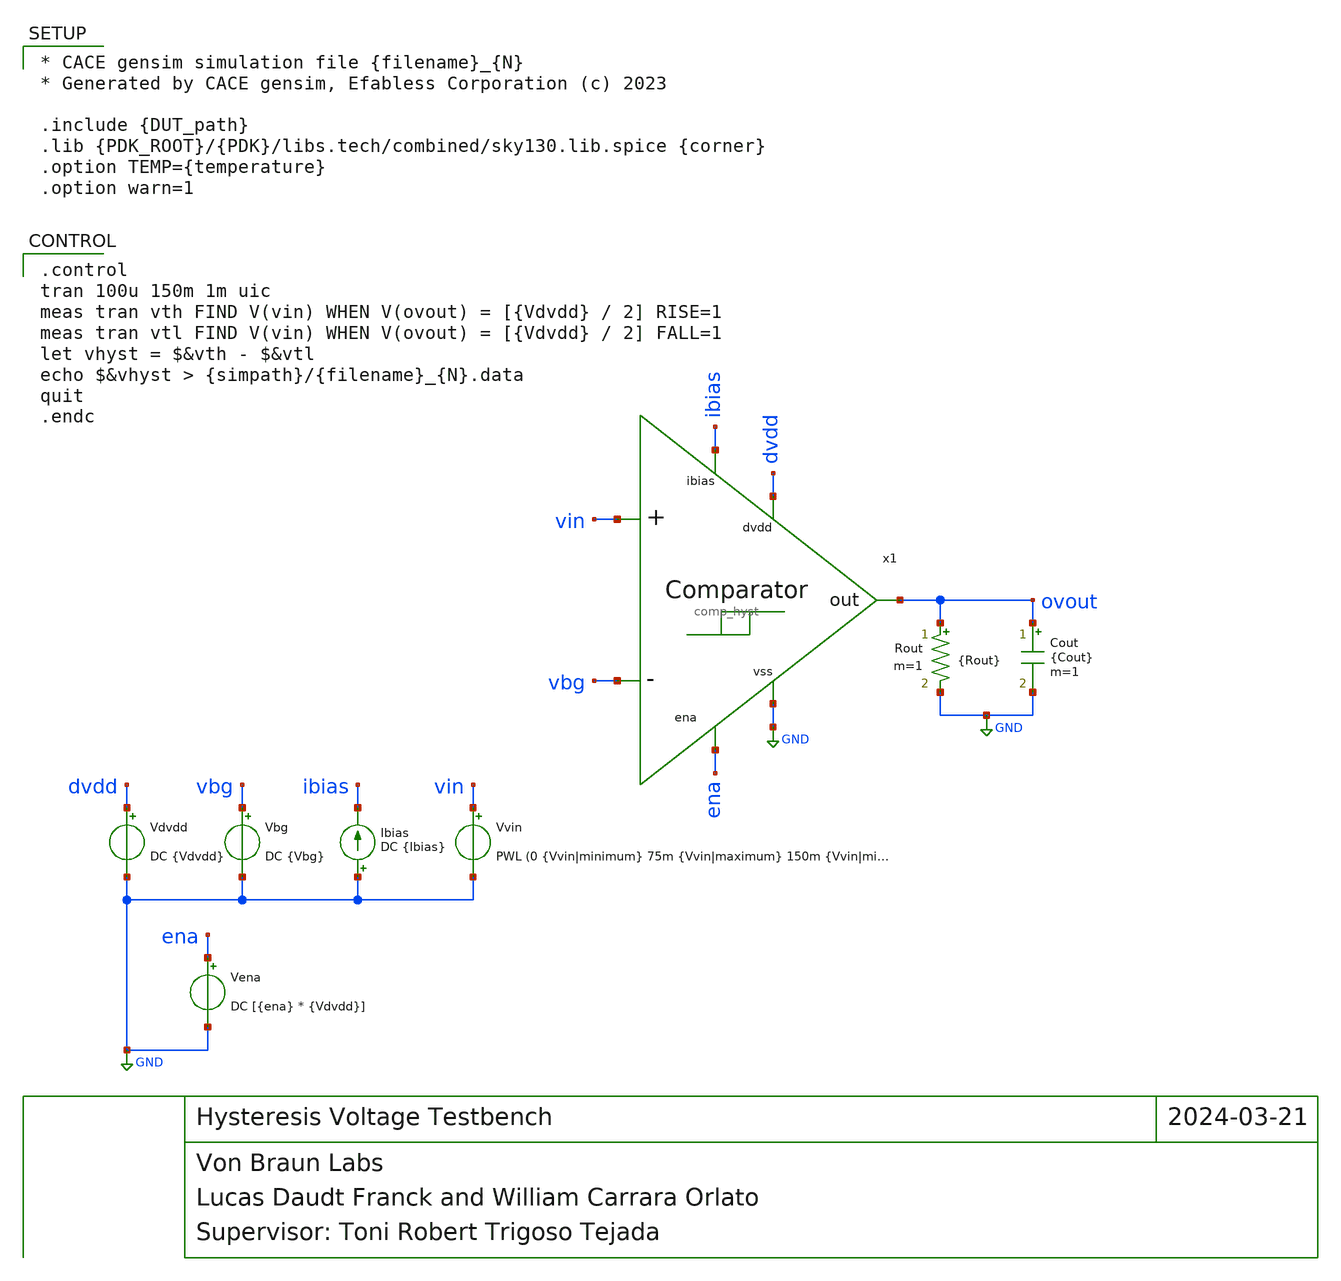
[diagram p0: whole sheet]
** sch_path: blocks/comp_hyst/cace/tb_vhyst.sch
* blocks/comp_hyst/xschem/comp_hyst.sch:
* Design under the Apache License Version 2.0 (Jan. 2004)
**.subckt tb_vhyst
Vvin vin GND PWL (0 {Vvin|minimum} 75m {Vvin|maximum} 150m {Vvin|minimum})
Vdvdd dvdd GND DC {Vdvdd}
Vbg vbg GND DC {Vbg}
Ibias GND ibias DC {Ibias}
Vena ena GND DC [{ena} * {Vdvdd}]
Cout ovout GND {Cout} m=1
Rout ovout GND {Rout} m=1
x1 dvdd ovout vbg vin ena ibias GND comp_hyst
**** begin user architecture code

* CACE gensim simulation file {filename}_{N}
* Generated by CACE gensim, Efabless Corporation (c) 2023

.include {DUT_path}
.lib {PDK_ROOT}/{PDK}/libs.tech/combined/sky130.lib.spice {corner}
.option TEMP={temperature}
.option warn=1



.control
tran 100u 150m 1m uic
meas tran vth FIND V(vin) WHEN V(ovout) = [{Vdvdd} / 2] RISE=1
meas tran vtl FIND V(vin) WHEN V(ovout) = [{Vdvdd} / 2] FALL=1
let vhyst = $&vth - $&vtl
echo $&vhyst > {simpath}/{filename}_{N}.data
quit
.endc


**** end user architecture code
**.ends

* expanding   symbol:  /home/vblabs/Music/blocks/comp_hyst/xschem/comp_hyst.sym # of pins=7
** sym_path: blocks/comp_hyst/xschem/comp_hyst.sym
** sch_path: blocks/comp_hyst/xschem/comp_hyst.sch
.subckt comp_hyst dvdd out vref vin ena ibias vss
*.iopin dvdd
*.ipin vref
*.ipin vin
*.opin out
*.ipin ibias
*.ipin ena
*.iopin vss
XM5[0] net3 net4 dvdd dvdd sky130_fd_pr__pfet_01v8 L=8 W=1 nf=1 ad='int((nf+1)/2) * W/nf * 0.29' as='int((nf+2)/2) * W/nf * 0.29'
+ pd='2*int((nf+1)/2) * (W/nf + 0.29)' ps='2*int((nf+2)/2) * (W/nf + 0.29)' nrd='0.29 / W' nrs='0.29 / W'
+ sa=0 sb=0 sd=0 mult=1 m=1
XM5[1] net3 net4 dvdd dvdd sky130_fd_pr__pfet_01v8 L=8 W=1 nf=1 ad='int((nf+1)/2) * W/nf * 0.29' as='int((nf+2)/2) * W/nf * 0.29'
+ pd='2*int((nf+1)/2) * (W/nf + 0.29)' ps='2*int((nf+2)/2) * (W/nf + 0.29)' nrd='0.29 / W' nrs='0.29 / W'
+ sa=0 sb=0 sd=0 mult=1 m=1
XM2[0] net4 net4 dvdd dvdd sky130_fd_pr__pfet_01v8 L=8 W=1 nf=1 ad='int((nf+1)/2) * W/nf * 0.29' as='int((nf+2)/2) * W/nf * 0.29'
+ pd='2*int((nf+1)/2) * (W/nf + 0.29)' ps='2*int((nf+2)/2) * (W/nf + 0.29)' nrd='0.29 / W' nrs='0.29 / W'
+ sa=0 sb=0 sd=0 mult=1 m=1
XM2[1] net4 net4 dvdd dvdd sky130_fd_pr__pfet_01v8 L=8 W=1 nf=1 ad='int((nf+1)/2) * W/nf * 0.29' as='int((nf+2)/2) * W/nf * 0.29'
+ pd='2*int((nf+1)/2) * (W/nf + 0.29)' ps='2*int((nf+2)/2) * (W/nf + 0.29)' nrd='0.29 / W' nrs='0.29 / W'
+ sa=0 sb=0 sd=0 mult=1 m=1
XM8 net2 net4 dvdd dvdd sky130_fd_pr__pfet_01v8 L=8 W=1 nf=1 ad='int((nf+1)/2) * W/nf * 0.29' as='int((nf+2)/2) * W/nf * 0.29'
+ pd='2*int((nf+1)/2) * (W/nf + 0.29)' ps='2*int((nf+2)/2) * (W/nf + 0.29)' nrd='0.29 / W' nrs='0.29 / W'
+ sa=0 sb=0 sd=0 mult=1 m=1
XM10[0] net3 net3 dvdd dvdd sky130_fd_pr__pfet_01v8 L=16 W=1 nf=1 ad='int((nf+1)/2) * W/nf * 0.29' as='int((nf+2)/2) * W/nf * 0.29'
+ pd='2*int((nf+1)/2) * (W/nf + 0.29)' ps='2*int((nf+2)/2) * (W/nf + 0.29)' nrd='0.29 / W' nrs='0.29 / W'
+ sa=0 sb=0 sd=0 mult=1 m=1
XM10[1] net3 net3 dvdd dvdd sky130_fd_pr__pfet_01v8 L=16 W=1 nf=1 ad='int((nf+1)/2) * W/nf * 0.29' as='int((nf+2)/2) * W/nf * 0.29'
+ pd='2*int((nf+1)/2) * (W/nf + 0.29)' ps='2*int((nf+2)/2) * (W/nf + 0.29)' nrd='0.29 / W' nrs='0.29 / W'
+ sa=0 sb=0 sd=0 mult=1 m=1
XM11 net5 net5 vss vss sky130_fd_pr__nfet_01v8 L=20 W=1 nf=1 ad='int((nf+1)/2) * W/nf * 0.29' as='int((nf+2)/2) * W/nf * 0.29'
+ pd='2*int((nf+1)/2) * (W/nf + 0.29)' ps='2*int((nf+2)/2) * (W/nf + 0.29)' nrd='0.29 / W' nrs='0.29 / W'
+ sa=0 sb=0 sd=0 mult=1 m=1
XM12 net1 net5 vss vss sky130_fd_pr__nfet_01v8 L=20 W=1 nf=1 ad='int((nf+1)/2) * W/nf * 0.29' as='int((nf+2)/2) * W/nf * 0.29'
+ pd='2*int((nf+1)/2) * (W/nf + 0.29)' ps='2*int((nf+2)/2) * (W/nf + 0.29)' nrd='0.29 / W' nrs='0.29 / W'
+ sa=0 sb=0 sd=0 mult=1 m=1
XM4 out net3 dvdd dvdd sky130_fd_pr__pfet_01v8 L=1 W=3 nf=1 ad='int((nf+1)/2) * W/nf * 0.29' as='int((nf+2)/2) * W/nf * 0.29'
+ pd='2*int((nf+1)/2) * (W/nf + 0.29)' ps='2*int((nf+2)/2) * (W/nf + 0.29)' nrd='0.29 / W' nrs='0.29 / W'
+ sa=0 sb=0 sd=0 mult=1 m=1
XM13 out net2 vss vss sky130_fd_pr__nfet_01v8 L=1 W=3 nf=1 ad='int((nf+1)/2) * W/nf * 0.29' as='int((nf+2)/2) * W/nf * 0.29'
+ pd='2*int((nf+1)/2) * (W/nf + 0.29)' ps='2*int((nf+2)/2) * (W/nf + 0.29)' nrd='0.29 / W' nrs='0.29 / W'
+ sa=0 sb=0 sd=0 mult=1 m=1
XM20 out ena_b vss vss sky130_fd_pr__nfet_01v8 L=3 W=1 nf=1 ad='int((nf+1)/2) * W/nf * 0.29' as='int((nf+2)/2) * W/nf * 0.29'
+ pd='2*int((nf+1)/2) * (W/nf + 0.29)' ps='2*int((nf+2)/2) * (W/nf + 0.29)' nrd='0.29 / W' nrs='0.29 / W'
+ sa=0 sb=0 sd=0 mult=1 m=1
XM3[0] net4 vref net1 vss sky130_fd_pr__nfet_g5v0d10v5 L=10 W=4 nf=1 ad='int((nf+1)/2) * W/nf * 0.29'
+ as='int((nf+2)/2) * W/nf * 0.29' pd='2*int((nf+1)/2) * (W/nf + 0.29)' ps='2*int((nf+2)/2) * (W/nf + 0.29)'
+ nrd='0.29 / W' nrs='0.29 / W' sa=0 sb=0 sd=0 mult=1 m=1
XM3[1] net4 vref net1 vss sky130_fd_pr__nfet_g5v0d10v5 L=10 W=4 nf=1 ad='int((nf+1)/2) * W/nf * 0.29'
+ as='int((nf+2)/2) * W/nf * 0.29' pd='2*int((nf+1)/2) * (W/nf + 0.29)' ps='2*int((nf+2)/2) * (W/nf + 0.29)'
+ nrd='0.29 / W' nrs='0.29 / W' sa=0 sb=0 sd=0 mult=1 m=1
XM3[2] net4 vref net1 vss sky130_fd_pr__nfet_g5v0d10v5 L=10 W=4 nf=1 ad='int((nf+1)/2) * W/nf * 0.29'
+ as='int((nf+2)/2) * W/nf * 0.29' pd='2*int((nf+1)/2) * (W/nf + 0.29)' ps='2*int((nf+2)/2) * (W/nf + 0.29)'
+ nrd='0.29 / W' nrs='0.29 / W' sa=0 sb=0 sd=0 mult=1 m=1
XM3[3] net4 vref net1 vss sky130_fd_pr__nfet_g5v0d10v5 L=10 W=4 nf=1 ad='int((nf+1)/2) * W/nf * 0.29'
+ as='int((nf+2)/2) * W/nf * 0.29' pd='2*int((nf+1)/2) * (W/nf + 0.29)' ps='2*int((nf+2)/2) * (W/nf + 0.29)'
+ nrd='0.29 / W' nrs='0.29 / W' sa=0 sb=0 sd=0 mult=1 m=1
XM4[0] net3 vin net1 vss sky130_fd_pr__nfet_g5v0d10v5 L=10 W=4 nf=1 ad='int((nf+1)/2) * W/nf * 0.29'
+ as='int((nf+2)/2) * W/nf * 0.29' pd='2*int((nf+1)/2) * (W/nf + 0.29)' ps='2*int((nf+2)/2) * (W/nf + 0.29)'
+ nrd='0.29 / W' nrs='0.29 / W' sa=0 sb=0 sd=0 mult=1 m=1
XM4[1] net3 vin net1 vss sky130_fd_pr__nfet_g5v0d10v5 L=10 W=4 nf=1 ad='int((nf+1)/2) * W/nf * 0.29'
+ as='int((nf+2)/2) * W/nf * 0.29' pd='2*int((nf+1)/2) * (W/nf + 0.29)' ps='2*int((nf+2)/2) * (W/nf + 0.29)'
+ nrd='0.29 / W' nrs='0.29 / W' sa=0 sb=0 sd=0 mult=1 m=1
XM4[2] net3 vin net1 vss sky130_fd_pr__nfet_g5v0d10v5 L=10 W=4 nf=1 ad='int((nf+1)/2) * W/nf * 0.29'
+ as='int((nf+2)/2) * W/nf * 0.29' pd='2*int((nf+1)/2) * (W/nf + 0.29)' ps='2*int((nf+2)/2) * (W/nf + 0.29)'
+ nrd='0.29 / W' nrs='0.29 / W' sa=0 sb=0 sd=0 mult=1 m=1
XM4[3] net3 vin net1 vss sky130_fd_pr__nfet_g5v0d10v5 L=10 W=4 nf=1 ad='int((nf+1)/2) * W/nf * 0.29'
+ as='int((nf+2)/2) * W/nf * 0.29' pd='2*int((nf+1)/2) * (W/nf + 0.29)' ps='2*int((nf+2)/2) * (W/nf + 0.29)'
+ nrd='0.29 / W' nrs='0.29 / W' sa=0 sb=0 sd=0 mult=1 m=1
XM3 net5 ena_b vss vss sky130_fd_pr__nfet_01v8 L=3 W=1 nf=1 ad='int((nf+1)/2) * W/nf * 0.29' as='int((nf+2)/2) * W/nf * 0.29'
+ pd='2*int((nf+1)/2) * (W/nf + 0.29)' ps='2*int((nf+2)/2) * (W/nf + 0.29)' nrd='0.29 / W' nrs='0.29 / W'
+ sa=0 sb=0 sd=0 mult=1 m=1
XM1[0] net4 net3 dvdd dvdd sky130_fd_pr__pfet_01v8 L=16 W=1 nf=1 ad='int((nf+1)/2) * W/nf * 0.29' as='int((nf+2)/2) * W/nf * 0.29'
+ pd='2*int((nf+1)/2) * (W/nf + 0.29)' ps='2*int((nf+2)/2) * (W/nf + 0.29)' nrd='0.29 / W' nrs='0.29 / W'
+ sa=0 sb=0 sd=0 mult=1 m=1
XM1[1] net4 net3 dvdd dvdd sky130_fd_pr__pfet_01v8 L=16 W=1 nf=1 ad='int((nf+1)/2) * W/nf * 0.29' as='int((nf+2)/2) * W/nf * 0.29'
+ pd='2*int((nf+1)/2) * (W/nf + 0.29)' ps='2*int((nf+2)/2) * (W/nf + 0.29)' nrd='0.29 / W' nrs='0.29 / W'
+ sa=0 sb=0 sd=0 mult=1 m=1
XM1[2] net4 net3 dvdd dvdd sky130_fd_pr__pfet_01v8 L=16 W=1 nf=1 ad='int((nf+1)/2) * W/nf * 0.29' as='int((nf+2)/2) * W/nf * 0.29'
+ pd='2*int((nf+1)/2) * (W/nf + 0.29)' ps='2*int((nf+2)/2) * (W/nf + 0.29)' nrd='0.29 / W' nrs='0.29 / W'
+ sa=0 sb=0 sd=0 mult=1 m=1
XM1[3] net4 net3 dvdd dvdd sky130_fd_pr__pfet_01v8 L=16 W=1 nf=1 ad='int((nf+1)/2) * W/nf * 0.29' as='int((nf+2)/2) * W/nf * 0.29'
+ pd='2*int((nf+1)/2) * (W/nf + 0.29)' ps='2*int((nf+2)/2) * (W/nf + 0.29)' nrd='0.29 / W' nrs='0.29 / W'
+ sa=0 sb=0 sd=0 mult=1 m=1
XM1[4] net4 net3 dvdd dvdd sky130_fd_pr__pfet_01v8 L=16 W=1 nf=1 ad='int((nf+1)/2) * W/nf * 0.29' as='int((nf+2)/2) * W/nf * 0.29'
+ pd='2*int((nf+1)/2) * (W/nf + 0.29)' ps='2*int((nf+2)/2) * (W/nf + 0.29)' nrd='0.29 / W' nrs='0.29 / W'
+ sa=0 sb=0 sd=0 mult=1 m=1
XM1[5] net4 net3 dvdd dvdd sky130_fd_pr__pfet_01v8 L=16 W=1 nf=1 ad='int((nf+1)/2) * W/nf * 0.29' as='int((nf+2)/2) * W/nf * 0.29'
+ pd='2*int((nf+1)/2) * (W/nf + 0.29)' ps='2*int((nf+2)/2) * (W/nf + 0.29)' nrd='0.29 / W' nrs='0.29 / W'
+ sa=0 sb=0 sd=0 mult=1 m=1
XM9 net2 net2 vss vss sky130_fd_pr__nfet_01v8 L=8 W=1 nf=1 ad='int((nf+1)/2) * W/nf * 0.29' as='int((nf+2)/2) * W/nf * 0.29'
+ pd='2*int((nf+1)/2) * (W/nf + 0.29)' ps='2*int((nf+2)/2) * (W/nf + 0.29)' nrd='0.29 / W' nrs='0.29 / W'
+ sa=0 sb=0 sd=0 mult=1 m=1
XM5 net3 ena dvdd dvdd sky130_fd_pr__pfet_01v8 L=3 W=1 nf=1 ad='int((nf+1)/2) * W/nf * 0.29' as='int((nf+2)/2) * W/nf * 0.29'
+ pd='2*int((nf+1)/2) * (W/nf + 0.29)' ps='2*int((nf+2)/2) * (W/nf + 0.29)' nrd='0.29 / W' nrs='0.29 / W'
+ sa=0 sb=0 sd=0 mult=1 m=1
XM14 net4 ena dvdd dvdd sky130_fd_pr__pfet_01v8 L=3 W=1 nf=1 ad='int((nf+1)/2) * W/nf * 0.29' as='int((nf+2)/2) * W/nf * 0.29'
+ pd='2*int((nf+1)/2) * (W/nf + 0.29)' ps='2*int((nf+2)/2) * (W/nf + 0.29)' nrd='0.29 / W' nrs='0.29 / W'
+ sa=0 sb=0 sd=0 mult=1 m=1
XM15 net2 ena_b vss vss sky130_fd_pr__nfet_01v8 L=3 W=1 nf=1 ad='int((nf+1)/2) * W/nf * 0.29' as='int((nf+2)/2) * W/nf * 0.29'
+ pd='2*int((nf+1)/2) * (W/nf + 0.29)' ps='2*int((nf+2)/2) * (W/nf + 0.29)' nrd='0.29 / W' nrs='0.29 / W'
+ sa=0 sb=0 sd=0 mult=1 m=1
XM1 ena_b ena dvdd dvdd sky130_fd_pr__pfet_01v8 L=3 W=1 nf=1 ad='int((nf+1)/2) * W/nf * 0.29' as='int((nf+2)/2) * W/nf * 0.29'
+ pd='2*int((nf+1)/2) * (W/nf + 0.29)' ps='2*int((nf+2)/2) * (W/nf + 0.29)' nrd='0.29 / W' nrs='0.29 / W'
+ sa=0 sb=0 sd=0 mult=1 m=1
XM2 ena_b ena vss vss sky130_fd_pr__nfet_01v8 L=3 W=1 nf=1 ad='int((nf+1)/2) * W/nf * 0.29' as='int((nf+2)/2) * W/nf * 0.29'
+ pd='2*int((nf+1)/2) * (W/nf + 0.29)' ps='2*int((nf+2)/2) * (W/nf + 0.29)' nrd='0.29 / W' nrs='0.29 / W'
+ sa=0 sb=0 sd=0 mult=1 m=1
x1 ibias ena ena_b dvdd vss net5 trans_gate
.ends


* expanding   symbol:  trans_gate.sym # of pins=6
** sym_path: blocks/comp_hyst/xschem/trans_gate.sym
** sch_path: blocks/comp_hyst/xschem/trans_gate.sch
.subckt trans_gate in ena_b ena avdd vss out
*.iopin avdd
*.iopin vss
*.ipin ena
*.ipin ena_b
*.ipin in
*.ipin out
XM1 in ena_b out vss sky130_fd_pr__nfet_g5v0d10v5 L=5 W=1 nf=1 ad='int((nf+1)/2) * W/nf * 0.29' as='int((nf+2)/2) * W/nf * 0.29'
+ pd='2*int((nf+1)/2) * (W/nf + 0.29)' ps='2*int((nf+2)/2) * (W/nf + 0.29)' nrd='0.29 / W' nrs='0.29 / W'
+ sa=0 sb=0 sd=0 mult=1 m=1
XM2 in ena out avdd sky130_fd_pr__pfet_g5v0d10v5 L=5 W=6 nf=1 ad='int((nf+1)/2) * W/nf * 0.29' as='int((nf+2)/2) * W/nf * 0.29'
+ pd='2*int((nf+1)/2) * (W/nf + 0.29)' ps='2*int((nf+2)/2) * (W/nf + 0.29)' nrd='0.29 / W' nrs='0.29 / W'
+ sa=0 sb=0 sd=0 mult=1 m=1
.ends

.GLOBAL GND
.end
